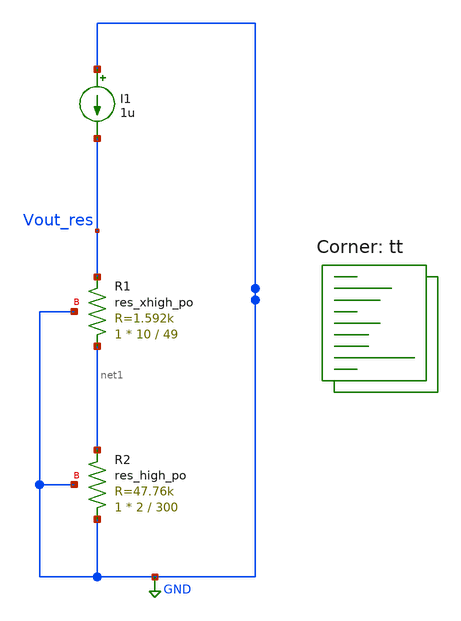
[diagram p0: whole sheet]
** sch_path: xschem/misc/testing/res_current_ref.sch
**.subckt res_current_ref
I1 GND Vout_res 1u
XR2 GND net1 GND sky130_fd_pr__res_high_po W=2 L=300 mult=1 m=1
XR1 net1 Vout_res GND sky130_fd_pr__res_xhigh_po W=10 L=49 mult=1 m=1
**** begin user architecture code
.lib $::SKYWATER_MODELS/sky130.lib.spice tt


.param temp=27

.dc temp -40 125 1


.save all
.control
run
plot Vout_res
plot deriv(Vout_res)
.endc



**** end user architecture code
**.ends
.GLOBAL GND
.end
